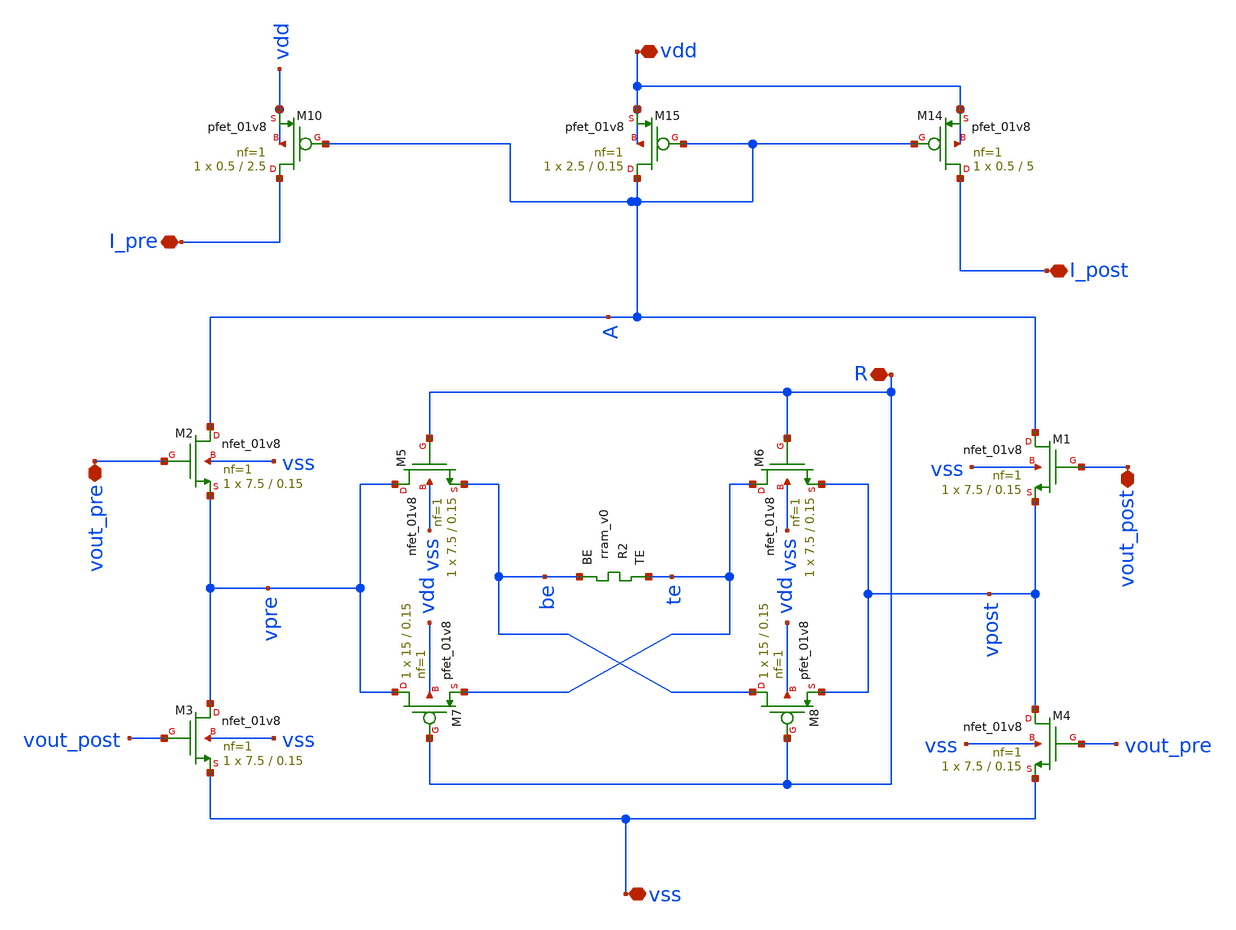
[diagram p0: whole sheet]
** sch_path: Synapse/rstdp_mirror_two_outs.sch
**.subckt rstdp_mirror_two_outs vdd vss R vout_post vout_pre I_post I_pre
*.iopin vdd
*.iopin vss
*.iopin R
*.iopin vout_post
*.iopin vout_pre
*.iopin I_post
*.iopin I_pre
XM2 A vout_pre vpre vss sky130_fd_pr__nfet_01v8 L=0.15 W=7.5 nf=1 ad='int((nf+1)/2) * W/nf * 0.29' as='int((nf+2)/2) * W/nf * 0.29'
+ pd='2*int((nf+1)/2) * (W/nf + 0.29)' ps='2*int((nf+2)/2) * (W/nf + 0.29)' nrd='0.29 / W' nrs='0.29 / W'
+ sa=0 sb=0 sd=0 mult=1 m=1
XM3 vpre vout_post vss vss sky130_fd_pr__nfet_01v8 L=0.15 W=7.5 nf=1 ad='int((nf+1)/2) * W/nf * 0.29'
+ as='int((nf+2)/2) * W/nf * 0.29' pd='2*int((nf+1)/2) * (W/nf + 0.29)' ps='2*int((nf+2)/2) * (W/nf + 0.29)'
+ nrd='0.29 / W' nrs='0.29 / W' sa=0 sb=0 sd=0 mult=1 m=1
XM1 A vout_post vpost vss sky130_fd_pr__nfet_01v8 L=0.15 W=7.5 nf=1 ad='int((nf+1)/2) * W/nf * 0.29'
+ as='int((nf+2)/2) * W/nf * 0.29' pd='2*int((nf+1)/2) * (W/nf + 0.29)' ps='2*int((nf+2)/2) * (W/nf + 0.29)'
+ nrd='0.29 / W' nrs='0.29 / W' sa=0 sb=0 sd=0 mult=1 m=1
XM4 vpost vout_pre vss vss sky130_fd_pr__nfet_01v8 L=0.15 W=7.5 nf=1 ad='int((nf+1)/2) * W/nf * 0.29'
+ as='int((nf+2)/2) * W/nf * 0.29' pd='2*int((nf+1)/2) * (W/nf + 0.29)' ps='2*int((nf+2)/2) * (W/nf + 0.29)'
+ nrd='0.29 / W' nrs='0.29 / W' sa=0 sb=0 sd=0 mult=1 m=1
XM10 I_pre A vdd vdd sky130_fd_pr__pfet_01v8 L=2.5 W=0.5 nf=1 ad='int((nf+1)/2) * W/nf * 0.29' as='int((nf+2)/2) * W/nf * 0.29'
+ pd='2*int((nf+1)/2) * (W/nf + 0.29)' ps='2*int((nf+2)/2) * (W/nf + 0.29)' nrd='0.29 / W' nrs='0.29 / W'
+ sa=0 sb=0 sd=0 mult=1 m=1
XR2 te be rram_v0
XM5 vpre R be vss sky130_fd_pr__nfet_01v8 L=0.15 W=7.5 nf=1 ad='int((nf+1)/2) * W/nf * 0.29' as='int((nf+2)/2) * W/nf * 0.29'
+ pd='2*int((nf+1)/2) * (W/nf + 0.29)' ps='2*int((nf+2)/2) * (W/nf + 0.29)' nrd='0.29 / W' nrs='0.29 / W'
+ sa=0 sb=0 sd=0 mult=1 m=1
XM6 te R vpost vss sky130_fd_pr__nfet_01v8 L=0.15 W=7.5 nf=1 ad='int((nf+1)/2) * W/nf * 0.29' as='int((nf+2)/2) * W/nf * 0.29'
+ pd='2*int((nf+1)/2) * (W/nf + 0.29)' ps='2*int((nf+2)/2) * (W/nf + 0.29)' nrd='0.29 / W' nrs='0.29 / W'
+ sa=0 sb=0 sd=0 mult=1 m=1
XM7 vpre R te vdd sky130_fd_pr__pfet_01v8 L=0.15 W=15 nf=1 ad='int((nf+1)/2) * W/nf * 0.29' as='int((nf+2)/2) * W/nf * 0.29'
+ pd='2*int((nf+1)/2) * (W/nf + 0.29)' ps='2*int((nf+2)/2) * (W/nf + 0.29)' nrd='0.29 / W' nrs='0.29 / W'
+ sa=0 sb=0 sd=0 mult=1 m=1
XM8 be R vpost vdd sky130_fd_pr__pfet_01v8 L=0.15 W=15 nf=1 ad='int((nf+1)/2) * W/nf * 0.29' as='int((nf+2)/2) * W/nf * 0.29'
+ pd='2*int((nf+1)/2) * (W/nf + 0.29)' ps='2*int((nf+2)/2) * (W/nf + 0.29)' nrd='0.29 / W' nrs='0.29 / W'
+ sa=0 sb=0 sd=0 mult=1 m=1
XM14 I_post A vdd vdd sky130_fd_pr__pfet_01v8 L=5 W=0.5 nf=1 ad='int((nf+1)/2) * W/nf * 0.29' as='int((nf+2)/2) * W/nf * 0.29'
+ pd='2*int((nf+1)/2) * (W/nf + 0.29)' ps='2*int((nf+2)/2) * (W/nf + 0.29)' nrd='0.29 / W' nrs='0.29 / W'
+ sa=0 sb=0 sd=0 mult=1 m=1
XM15 A A vdd vdd sky130_fd_pr__pfet_01v8 L=0.15 W=2.5 nf=1 ad='int((nf+1)/2) * W/nf * 0.29' as='int((nf+2)/2) * W/nf * 0.29'
+ pd='2*int((nf+1)/2) * (W/nf + 0.29)' ps='2*int((nf+2)/2) * (W/nf + 0.29)' nrd='0.29 / W' nrs='0.29 / W'
+ sa=0 sb=0 sd=0 mult=1 m=1
**.ends
.end
